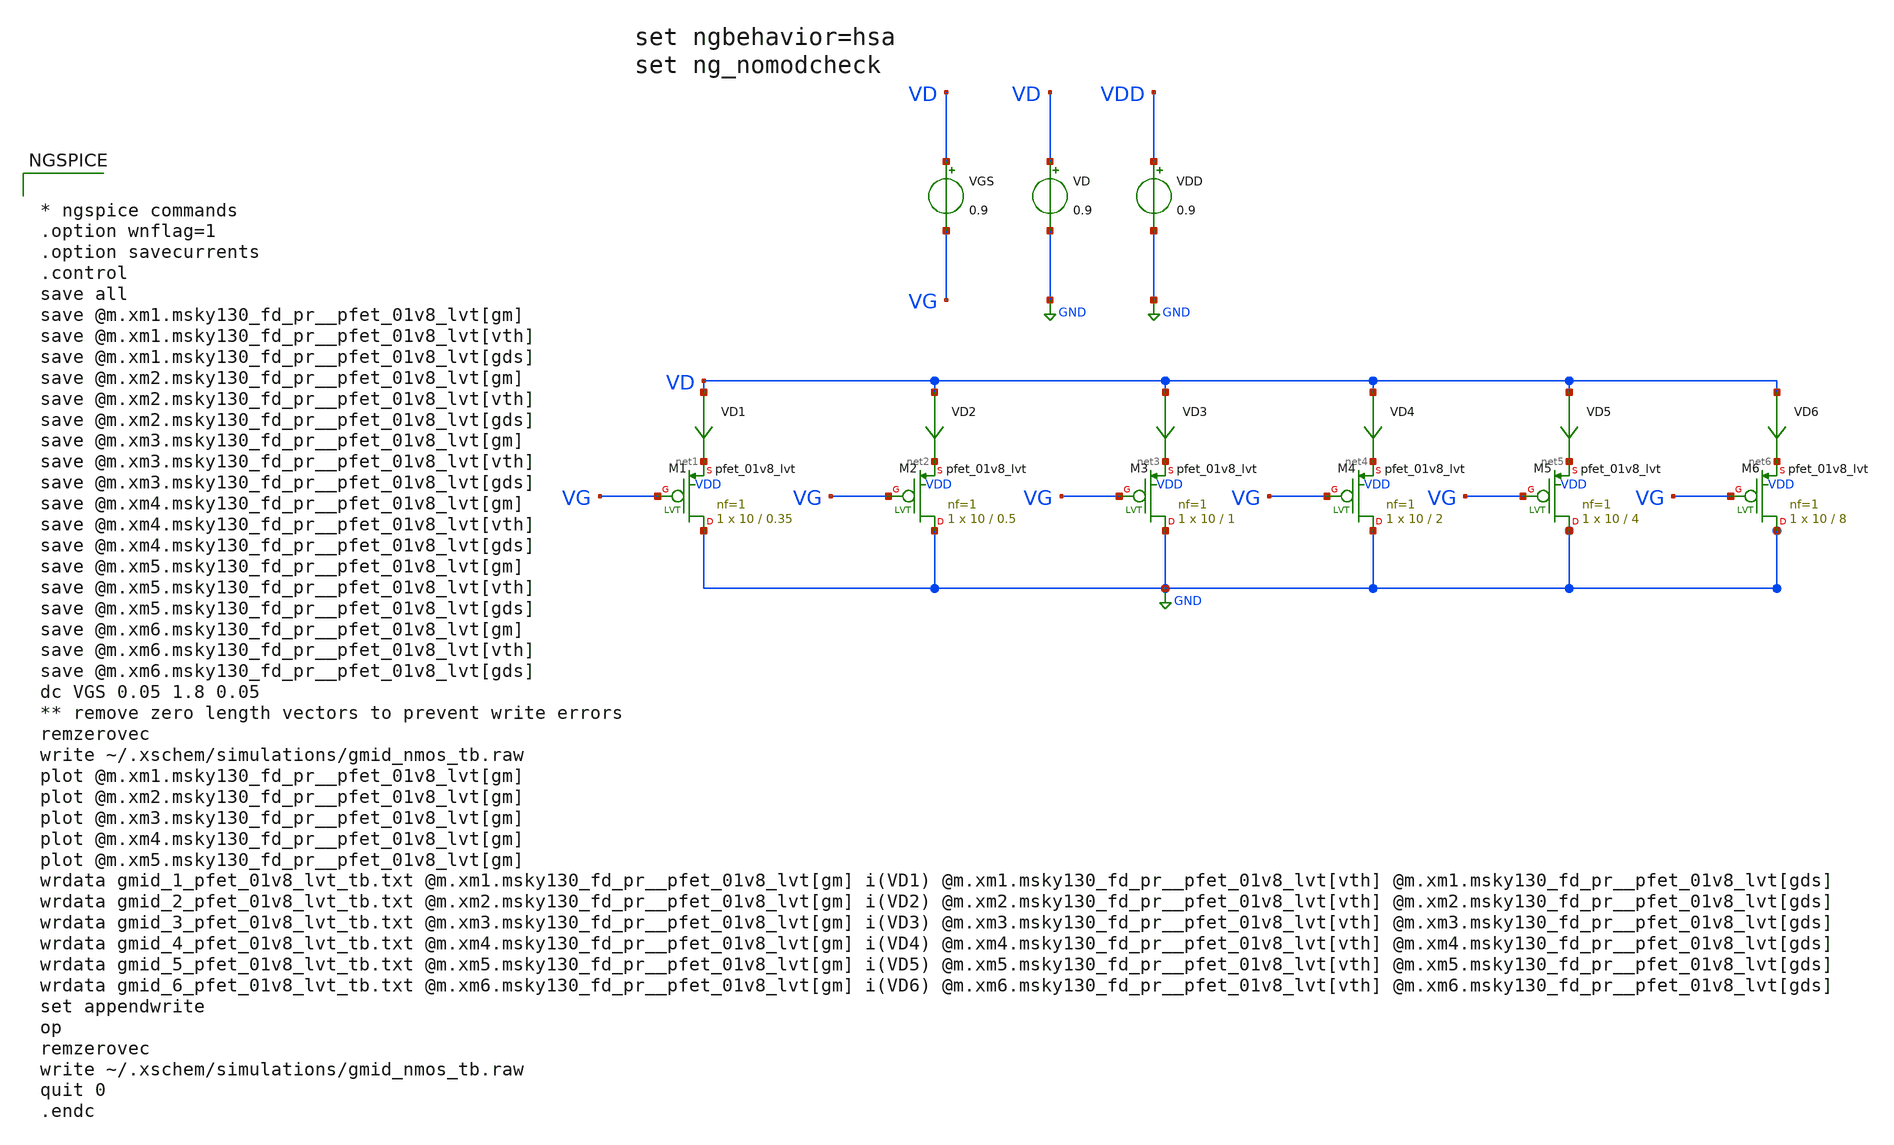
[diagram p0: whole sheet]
** sch_path: testbenches/gmid_pmos_1v8_lvt_tb.sch
**.subckt gmid_pmos_1v8_lvt_tb
VGS VD VG 0.9
VD VD GND 0.9
VD1 VD net1 0
.save i(vd1)
VD2 VD net2 0
.save i(vd2)
VD3 VD net3 0
.save i(vd3)
VD4 VD net4 0
.save i(vd4)
VD5 VD net5 0
.save i(vd5)
VDD VDD GND 0.9
XM1 GND VG net1 VDD sky130_fd_pr__pfet_01v8_lvt L=0.35 W=10 nf=1 ad='int((nf+1)/2) * W/nf * 0.29' as='int((nf+2)/2) * W/nf * 0.29'
+ pd='2*int((nf+1)/2) * (W/nf + 0.29)' ps='2*int((nf+2)/2) * (W/nf + 0.29)' nrd='0.29 / W' nrs='0.29 / W'
+ sa=0 sb=0 sd=0 mult=1 m=1
XM2 GND VG net2 VDD sky130_fd_pr__pfet_01v8_lvt L=0.5 W=10 nf=1 ad='int((nf+1)/2) * W/nf * 0.29' as='int((nf+2)/2) * W/nf * 0.29'
+ pd='2*int((nf+1)/2) * (W/nf + 0.29)' ps='2*int((nf+2)/2) * (W/nf + 0.29)' nrd='0.29 / W' nrs='0.29 / W'
+ sa=0 sb=0 sd=0 mult=1 m=1
XM3 GND VG net3 VDD sky130_fd_pr__pfet_01v8_lvt L=1 W=10 nf=1 ad='int((nf+1)/2) * W/nf * 0.29' as='int((nf+2)/2) * W/nf * 0.29'
+ pd='2*int((nf+1)/2) * (W/nf + 0.29)' ps='2*int((nf+2)/2) * (W/nf + 0.29)' nrd='0.29 / W' nrs='0.29 / W'
+ sa=0 sb=0 sd=0 mult=1 m=1
XM4 GND VG net4 VDD sky130_fd_pr__pfet_01v8_lvt L=2 W=10 nf=1 ad='int((nf+1)/2) * W/nf * 0.29' as='int((nf+2)/2) * W/nf * 0.29'
+ pd='2*int((nf+1)/2) * (W/nf + 0.29)' ps='2*int((nf+2)/2) * (W/nf + 0.29)' nrd='0.29 / W' nrs='0.29 / W'
+ sa=0 sb=0 sd=0 mult=1 m=1
XM5 GND VG net5 VDD sky130_fd_pr__pfet_01v8_lvt L=4 W=10 nf=1 ad='int((nf+1)/2) * W/nf * 0.29' as='int((nf+2)/2) * W/nf * 0.29'
+ pd='2*int((nf+1)/2) * (W/nf + 0.29)' ps='2*int((nf+2)/2) * (W/nf + 0.29)' nrd='0.29 / W' nrs='0.29 / W'
+ sa=0 sb=0 sd=0 mult=1 m=1
VD6 VD net6 0
.save i(vd6)
XM6 GND VG net6 VDD sky130_fd_pr__pfet_01v8_lvt L=8 W=10 nf=1 ad='int((nf+1)/2) * W/nf * 0.29' as='int((nf+2)/2) * W/nf * 0.29'
+ pd='2*int((nf+1)/2) * (W/nf + 0.29)' ps='2*int((nf+2)/2) * (W/nf + 0.29)' nrd='0.29 / W' nrs='0.29 / W'
+ sa=0 sb=0 sd=0 mult=1 m=1
**** begin user architecture code

** opencircuitdesign pdks install
.lib /foss/pdks/sky130A/libs.tech/ngspice/sky130.lib.corners.spice sshh



* ngspice commands
.option wnflag=1
.option savecurrents
.control
save all
save @m.xm1.msky130_fd_pr__pfet_01v8_lvt[gm]
save @m.xm1.msky130_fd_pr__pfet_01v8_lvt[vth]
save @m.xm1.msky130_fd_pr__pfet_01v8_lvt[gds]
save @m.xm2.msky130_fd_pr__pfet_01v8_lvt[gm]
save @m.xm2.msky130_fd_pr__pfet_01v8_lvt[vth]
save @m.xm2.msky130_fd_pr__pfet_01v8_lvt[gds]
save @m.xm3.msky130_fd_pr__pfet_01v8_lvt[gm]
save @m.xm3.msky130_fd_pr__pfet_01v8_lvt[vth]
save @m.xm3.msky130_fd_pr__pfet_01v8_lvt[gds]
save @m.xm4.msky130_fd_pr__pfet_01v8_lvt[gm]
save @m.xm4.msky130_fd_pr__pfet_01v8_lvt[vth]
save @m.xm4.msky130_fd_pr__pfet_01v8_lvt[gds]
save @m.xm5.msky130_fd_pr__pfet_01v8_lvt[gm]
save @m.xm5.msky130_fd_pr__pfet_01v8_lvt[vth]
save @m.xm5.msky130_fd_pr__pfet_01v8_lvt[gds]
save @m.xm6.msky130_fd_pr__pfet_01v8_lvt[gm]
save @m.xm6.msky130_fd_pr__pfet_01v8_lvt[vth]
save @m.xm6.msky130_fd_pr__pfet_01v8_lvt[gds]
dc VGS 0.05 1.8 0.05
** remove zero length vectors to prevent write errors
remzerovec
write ~/.xschem/simulations/gmid_nmos_tb.raw
plot @m.xm1.msky130_fd_pr__pfet_01v8_lvt[gm]
plot @m.xm2.msky130_fd_pr__pfet_01v8_lvt[gm]
plot @m.xm3.msky130_fd_pr__pfet_01v8_lvt[gm]
plot @m.xm4.msky130_fd_pr__pfet_01v8_lvt[gm]
plot @m.xm5.msky130_fd_pr__pfet_01v8_lvt[gm]
wrdata gmid_1_pfet_01v8_lvt_tb.txt @m.xm1.msky130_fd_pr__pfet_01v8_lvt[gm] i(VD1)
+ @m.xm1.msky130_fd_pr__pfet_01v8_lvt[vth] @m.xm1.msky130_fd_pr__pfet_01v8_lvt[gds]
wrdata gmid_2_pfet_01v8_lvt_tb.txt @m.xm2.msky130_fd_pr__pfet_01v8_lvt[gm] i(VD2)
+ @m.xm2.msky130_fd_pr__pfet_01v8_lvt[vth] @m.xm2.msky130_fd_pr__pfet_01v8_lvt[gds]
wrdata gmid_3_pfet_01v8_lvt_tb.txt @m.xm3.msky130_fd_pr__pfet_01v8_lvt[gm] i(VD3)
+ @m.xm3.msky130_fd_pr__pfet_01v8_lvt[vth] @m.xm3.msky130_fd_pr__pfet_01v8_lvt[gds]
wrdata gmid_4_pfet_01v8_lvt_tb.txt @m.xm4.msky130_fd_pr__pfet_01v8_lvt[gm] i(VD4)
+ @m.xm4.msky130_fd_pr__pfet_01v8_lvt[vth] @m.xm4.msky130_fd_pr__pfet_01v8_lvt[gds]
wrdata gmid_5_pfet_01v8_lvt_tb.txt @m.xm5.msky130_fd_pr__pfet_01v8_lvt[gm] i(VD5)
+ @m.xm5.msky130_fd_pr__pfet_01v8_lvt[vth] @m.xm5.msky130_fd_pr__pfet_01v8_lvt[gds]
wrdata gmid_6_pfet_01v8_lvt_tb.txt @m.xm6.msky130_fd_pr__pfet_01v8_lvt[gm] i(VD6)
+ @m.xm6.msky130_fd_pr__pfet_01v8_lvt[vth] @m.xm6.msky130_fd_pr__pfet_01v8_lvt[gds]
set appendwrite
op
remzerovec
write ~/.xschem/simulations/gmid_nmos_tb.raw
quit 0
.endc


**** end user architecture code
**.ends
.GLOBAL GND
.end
